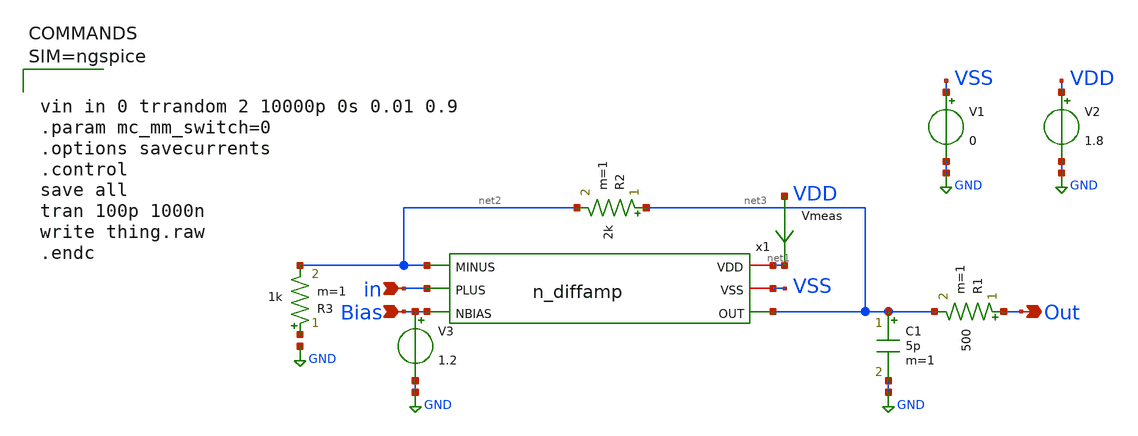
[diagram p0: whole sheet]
** sch_path: xschem/thing.sch
* xschem/n_diffamp.sch:
* Copyright 2021 Stefan Frederik Schippers
* Licensed under the Apache License, Version 2.0 (the "License");
**.subckt thing in Out Bias
*.ipin in
*.opin Out
*.ipin Bias
x1 net1 VSS net3 net2 in Bias n_diffamp
V1 VSS GND 0
V2 VDD GND 1.8
R1 Out net3 500 m=1
C1 net3 GND 5p m=1
V3 Bias GND 1.2
Vmeas VDD net1 0
R2 net3 net2 2k m=1
R3 net4 net2 1k m=1
**** begin user architecture code

** opencircuitdesign pdks install
.lib $::SKYWATER_MODELS/sky130.lib.spice tt





vin in 0 trrandom 2 10000p 0s 0.01 0.9
.param mc_mm_switch=0
.options savecurrents
.control
save all
tran 100p 1000n
write thing.raw
.endc



**** end user architecture code
**.ends

* expanding   symbol:  n_diffamp.sym # of pins=6
** sym_path: xschem/n_diffamp.sym
** sch_path: xschem/n_diffamp.sch
.subckt n_diffamp VDD VSS OUT MINUS PLUS NBIAS
*.ipin PLUS
*.ipin MINUS
*.opin OUT
*.ipin NBIAS
*.iopin VDD
*.iopin VSS
XM1 net1 PLUS S GND sky130_fd_pr__nfet_01v8_lvt L=0.3 W=2 nf=1 ad='int((nf+1)/2) * W/nf * 0.29' as='int((nf+2)/2) * W/nf * 0.29'
+ pd='2*int((nf+1)/2) * (W/nf + 0.29)' ps='2*int((nf+2)/2) * (W/nf + 0.29)' nrd='0.29 / W' nrs='0.29 / W'
+ sa=0 sb=0 sd=0 mult=1 m=1
XM2 OUT MINUS S GND sky130_fd_pr__nfet_01v8_lvt L=0.3 W=2 nf=1 ad='int((nf+1)/2) * W/nf * 0.29' as='int((nf+2)/2) * W/nf * 0.29'
+ pd='2*int((nf+1)/2) * (W/nf + 0.29)' ps='2*int((nf+2)/2) * (W/nf + 0.29)' nrd='0.29 / W' nrs='0.29 / W'
+ sa=0 sb=0 sd=0 mult=1 m=1
XM3 OUT net1 VDD VDD sky130_fd_pr__pfet_01v8_lvt L=0.8 W=4 nf=1 ad='int((nf+1)/2) * W/nf * 0.29' as='int((nf+2)/2) * W/nf * 0.29'
+ pd='2*int((nf+1)/2) * (W/nf + 0.29)' ps='2*int((nf+2)/2) * (W/nf + 0.29)' nrd='0.29 / W' nrs='0.29 / W'
+ sa=0 sb=0 sd=0 mult=1 m=1
XM4 net1 net1 VDD VDD sky130_fd_pr__pfet_01v8_lvt L=0.8 W=4 nf=1 ad='int((nf+1)/2) * W/nf * 0.29' as='int((nf+2)/2) * W/nf * 0.29'
+ pd='2*int((nf+1)/2) * (W/nf + 0.29)' ps='2*int((nf+2)/2) * (W/nf + 0.29)' nrd='0.29 / W' nrs='0.29 / W'
+ sa=0 sb=0 sd=0 mult=1 m=1
XM5 net2 NBIAS VSS GND sky130_fd_pr__nfet_01v8 L=1.2 W=0.7 nf=1 ad='int((nf+1)/2) * W/nf * 0.29' as='int((nf+2)/2) * W/nf * 0.29'
+ pd='2*int((nf+1)/2) * (W/nf + 0.29)' ps='2*int((nf+2)/2) * (W/nf + 0.29)' nrd='0.29 / W' nrs='0.29 / W'
+ sa=0 sb=0 sd=0 mult=1 m=1
XR1 VSS S VSS sky130_fd_pr__res_xhigh_po_0p35 L=50 mult=1 m=1
V5 S net2 0
.save i(v5)
.ends

.GLOBAL GND
.end
